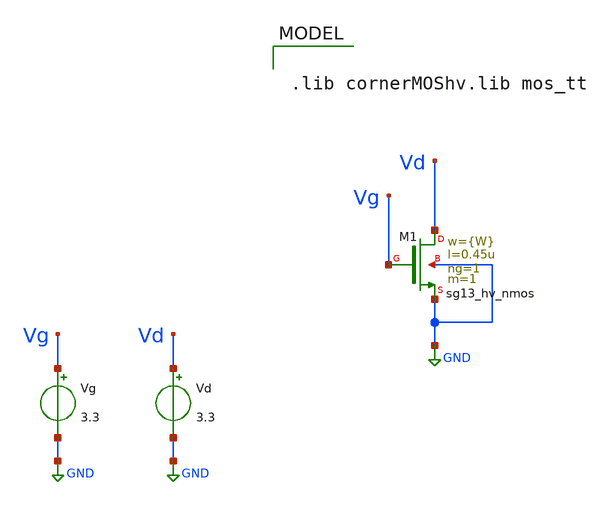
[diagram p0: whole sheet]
** sch_path: xschem/CMOS_Char/Ron_test.sch
**.subckt Ron_test
XM1 Vd Vg GND GND sg13_hv_nmos w={W} l=0.45u ng=1 m=1 mm_ok=1
Vg Vg GND 3.3
Vd Vd GND 3.3
**** begin user architecture code

.lib cornerMOShv.lib mos_tt




.param W = 1.0u
.param Vdd = 3.3




.control
let strt_w = 1.0u
let stop_w = 10u
let step_w = 0.1u
let curr_w = 1.0u
save all
while curr_w le stop_w
	alterparam W = $&curr_w
	reset
	save all
	+ @n.xm1.nsg13_hv_nmos[gds]
	op
	let rds = 1/@n.xm1.nsg13_hv_nmos[gds]
	wrdata ../top rds
	set appendwrite
	let curr_w = curr_w + step_w
end
.endc


**** end user architecture code
**.ends
.GLOBAL GND
.end
